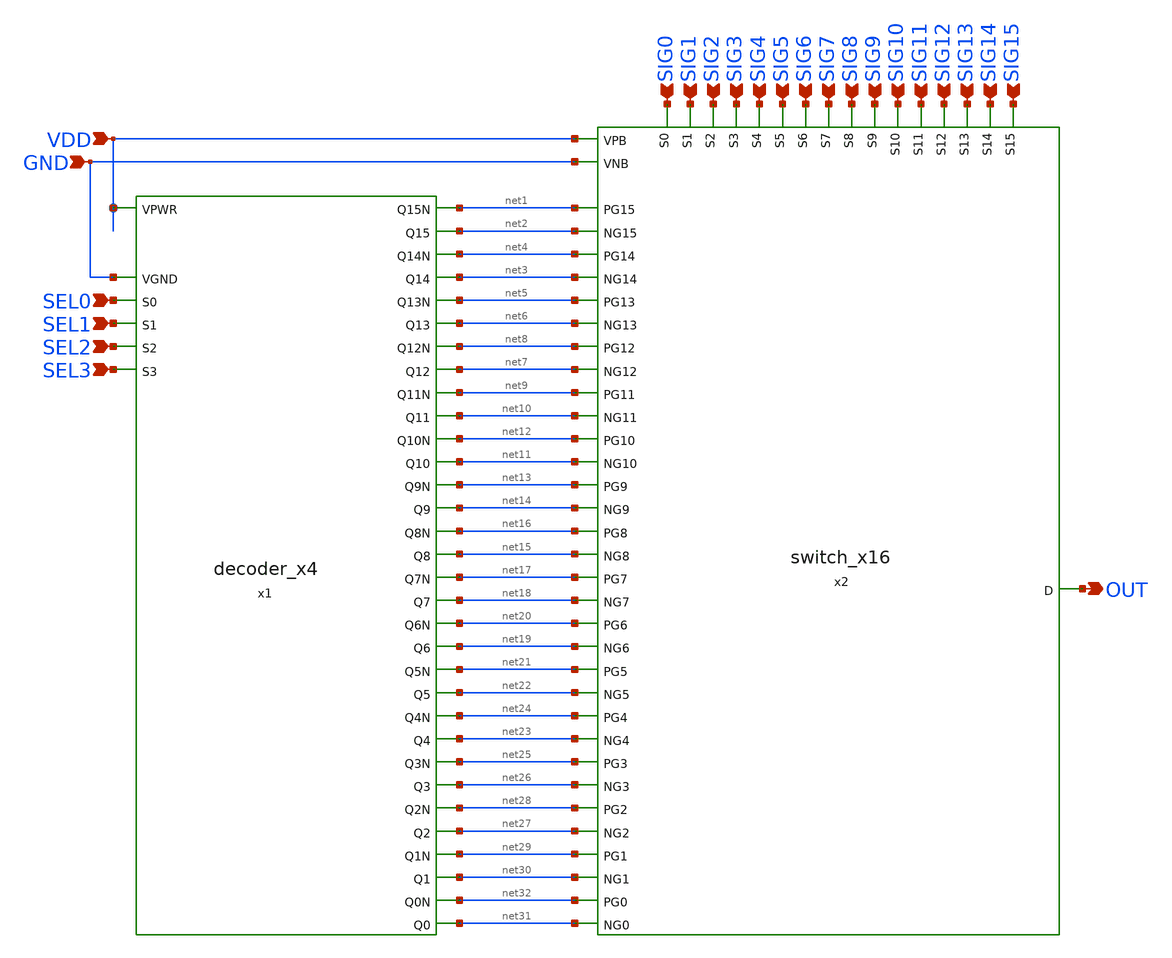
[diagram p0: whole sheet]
** sch_path: SP23_Tapeout/C2S2_Analog_TestChip-main/xschem/analog_mux.sch

.include $::SKYWATER_STDCELLS/sky130_fd_sc_hd.spice

**.subckt analog_mux OUT VDD GND SEL0 SEL1 SEL2 SEL3 SIG3 SIG2 SIG1 SIG0 SIG7 SIG6 SIG5 SIG4 SIG11
*+ SIG10 SIG9 SIG8 SIG15 SIG14 SIG13 SIG12
*.opin OUT
*.ipin VDD
*.ipin GND
*.ipin SEL0
*.ipin SEL1
*.ipin SEL2
*.ipin SEL3
*.ipin SIG3
*.ipin SIG2
*.ipin SIG1
*.ipin SIG0
*.ipin SIG7
*.ipin SIG6
*.ipin SIG5
*.ipin SIG4
*.ipin SIG11
*.ipin SIG10
*.ipin SIG9
*.ipin SIG8
*.ipin SIG15
*.ipin SIG14
*.ipin SIG13
*.ipin SIG12
x1 VDD GND SEL0 SEL1 SEL2 SEL3 net1 net2 net4 net3 net5 net6 net8 net7 net9 net10 net12 net11 net13
+ net14 net16 net15 net17 net18 net20 net19 net21 net22 net24 net23 net25 net26 net28 net27 net29 net30
+ net32 net31 decoder_x4
x2 SIG15 net1 net2 SIG14 net4 net3 SIG13 net5 net6 SIG12 net8 net7 SIG11 net9 net10 SIG10 net12
+ net11 SIG9 net13 net14 SIG8 net16 net15 OUT SIG7 net17 net18 SIG6 net20 net19 SIG5 net21 net22 SIG4 net24
+ net23 SIG3 net25 net26 SIG2 net28 net27 SIG1 net29 net30 SIG0 net32 net31 VDD GND switch_x16
**.ends

* expanding   symbol:  decoder_x4.sym # of pins=38
** sym_path: SP23_Tapeout/C2S2_Analog_TestChip-main/xschem/decoder_x4.sym
** sch_path: SP23_Tapeout/C2S2_Analog_TestChip-main/xschem/decoder_x4.sch
.subckt decoder_x4 VPWR VGND S0 S1 S2 S3 Q15N Q15 Q14N Q14 Q13N Q13 Q12N Q12 Q11N Q11 Q10N Q10 Q9N
+ Q9 Q8N Q8 Q7N Q7 Q6N Q6 Q5N Q5 Q4N Q4 Q3N Q3 Q2N Q2 Q1N Q1 Q0N Q0
*.ipin S3
*.ipin S2
*.ipin S1
*.ipin S0
*.ipin VGND
*.ipin VPWR
*.opin Q14N
*.opin Q15N
*.opin Q13N
*.opin Q12N
*.opin Q10N
*.opin Q11N
*.opin Q9N
*.opin Q8N
*.opin Q7N
*.opin Q6N
*.opin Q4N
*.opin Q3N
*.opin Q2N
*.opin Q1N
*.opin Q0N
*.opin Q5N
*.opin Q14
*.opin Q15
*.opin Q13
*.opin Q12
*.opin Q10
*.opin Q11
*.opin Q9
*.opin Q8
*.opin Q7
*.opin Q6
*.opin Q4
*.opin Q3
*.opin Q2
*.opin Q1
*.opin Q0
*.opin Q5
x17 S3 VGND VGND VPWR VPWR S3N sky130_fd_sc_hd__inv_8
x18 S2 VGND VGND VPWR VPWR S2N sky130_fd_sc_hd__inv_8
x19 S1 VGND VGND VPWR VPWR S1N sky130_fd_sc_hd__inv_8
x20 S0 VGND VGND VPWR VPWR S0N sky130_fd_sc_hd__inv_8
x21 Q0N VGND VGND VPWR VPWR Q0 sky130_fd_sc_hd__inv_2
x22 Q1N VGND VGND VPWR VPWR Q1 sky130_fd_sc_hd__inv_2
x23 Q2N VGND VGND VPWR VPWR Q2 sky130_fd_sc_hd__inv_2
x24 Q3N VGND VGND VPWR VPWR Q3 sky130_fd_sc_hd__inv_2
x1 S3N S2N S1N S0N VGND VGND VPWR VPWR Q0N sky130_fd_sc_hd__nand4_2
x2 S3N S2N S1N S0 VGND VGND VPWR VPWR Q1N sky130_fd_sc_hd__nand4_2
x3 S3N S2N S1 S0N VGND VGND VPWR VPWR Q2N sky130_fd_sc_hd__nand4_2
x4 S3N S2N S1 S0 VGND VGND VPWR VPWR Q3N sky130_fd_sc_hd__nand4_2
x5 S3N S2 S1N S0N VGND VGND VPWR VPWR Q4N sky130_fd_sc_hd__nand4_2
x6 S3N S2 S1N S0 VGND VGND VPWR VPWR Q5N sky130_fd_sc_hd__nand4_2
x7 S3N S2 S1 S0N VGND VGND VPWR VPWR Q6N sky130_fd_sc_hd__nand4_2
x8 S3N S2 S1 S0 VGND VGND VPWR VPWR Q7N sky130_fd_sc_hd__nand4_2
x9 S3 S2N S1N S0N VGND VGND VPWR VPWR Q8N sky130_fd_sc_hd__nand4_2
x10 S3 S2N S1N S0 VGND VGND VPWR VPWR Q9N sky130_fd_sc_hd__nand4_2
x11 S3 S2N S1 S0N VGND VGND VPWR VPWR Q10N sky130_fd_sc_hd__nand4_2
x12 S3 S2N S1 S0 VGND VGND VPWR VPWR Q11N sky130_fd_sc_hd__nand4_2
x13 S3 S2 S1N S0N VGND VGND VPWR VPWR Q12N sky130_fd_sc_hd__nand4_2
x14 S3 S2 S1N S0 VGND VGND VPWR VPWR Q13N sky130_fd_sc_hd__nand4_2
x15 S3 S2 S1 S0N VGND VGND VPWR VPWR Q14N sky130_fd_sc_hd__nand4_2
x16 S3 S2 S1 S0 VGND VGND VPWR VPWR Q15N sky130_fd_sc_hd__nand4_2
x25 Q4N VGND VGND VPWR VPWR Q4 sky130_fd_sc_hd__inv_2
x26 Q5N VGND VGND VPWR VPWR Q5 sky130_fd_sc_hd__inv_2
x27 Q6N VGND VGND VPWR VPWR Q6 sky130_fd_sc_hd__inv_2
x28 Q7N VGND VGND VPWR VPWR Q7 sky130_fd_sc_hd__inv_2
x29 Q8N VGND VGND VPWR VPWR Q8 sky130_fd_sc_hd__inv_2
x30 Q9N VGND VGND VPWR VPWR Q9 sky130_fd_sc_hd__inv_2
x31 Q10N VGND VGND VPWR VPWR Q10 sky130_fd_sc_hd__inv_2
x32 Q11N VGND VGND VPWR VPWR Q11 sky130_fd_sc_hd__inv_2
x33 Q12N VGND VGND VPWR VPWR Q12 sky130_fd_sc_hd__inv_2
x34 Q13N VGND VGND VPWR VPWR Q13 sky130_fd_sc_hd__inv_2
x35 Q14N VGND VGND VPWR VPWR Q14 sky130_fd_sc_hd__inv_2
x36 Q15N VGND VGND VPWR VPWR Q15 sky130_fd_sc_hd__inv_2
.ends


* expanding   symbol:  switch_x16.sym # of pins=51
** sym_path: switch_x16.sym
** sch_path: switch_x16.sch
.subckt switch_x16 S15 PG15 NG15 S14 PG14 NG14 S13 PG13 NG13 S12 PG12 NG12 S11 PG11 NG11 S10 PG10
+ NG10 S9 PG9 NG9 S8 PG8 NG8 D S7 PG7 NG7 S6 PG6 NG6 S5 PG5 NG5 S4 PG4 NG4 S3 PG3 NG3 S2 PG2 NG2 S1 PG1
+ NG1 S0 PG0 NG0 VPB VNB
*.ipin PG0
*.ipin NG0
*.ipin S0
*.ipin PG1
*.ipin NG1
*.ipin S1
*.ipin PG2
*.ipin NG2
*.ipin S2
*.ipin PG3
*.ipin NG3
*.ipin S3
*.ipin PG4
*.ipin NG4
*.ipin S4
*.ipin PG5
*.ipin NG5
*.ipin S5
*.ipin PG6
*.ipin NG6
*.ipin S6
*.ipin PG7
*.ipin NG7
*.ipin S7
*.ipin PG8
*.ipin NG8
*.ipin S8
*.ipin PG9
*.ipin NG9
*.ipin S9
*.ipin PG10
*.ipin NG10
*.ipin S10
*.ipin PG11
*.ipin NG11
*.ipin S11
*.ipin PG12
*.ipin NG12
*.ipin S12
*.ipin PG13
*.ipin NG13
*.ipin S13
*.ipin PG14
*.ipin NG14
*.ipin S14
*.ipin PG15
*.ipin NG15
*.ipin S15
*.opin D
*.ipin VPB
*.ipin VNB
x1 S0 VNB NG0 VPB PG0 D a_mux_switch
x2 S1 VNB NG1 VPB PG1 D a_mux_switch
x3 S2 VNB NG2 VPB PG2 D a_mux_switch
x4 S3 VNB NG3 VPB PG3 D a_mux_switch
x5 S4 VNB NG4 VPB PG4 D a_mux_switch
x6 S5 VNB NG5 VPB PG5 D a_mux_switch
x7 S6 VNB NG6 VPB PG6 D a_mux_switch
x8 S7 VNB NG7 VPB PG7 D a_mux_switch
x9 S8 VNB NG8 VPB PG8 D a_mux_switch
x10 S9 VNB NG9 VPB PG9 D a_mux_switch
x11 S10 VNB NG10 VPB PG10 D a_mux_switch
x15 S11 VNB NG11 VPB PG11 D a_mux_switch
x16 S12 VNB NG12 VPB PG12 D a_mux_switch
x17 S13 VNB NG13 VPB PG13 D a_mux_switch
x18 S14 VNB NG14 VPB PG14 D a_mux_switch
x19 S15 VNB NG15 VPB PG15 D a_mux_switch
.ends


* expanding   symbol:  a_mux_switch.sym # of pins=6
** sym_path: SP23_Tapeout/C2S2_Analog_TestChip-main/xschem/a_mux_switch.sym
** sch_path: SP23_Tapeout/C2S2_Analog_TestChip-main/xschem/a_mux_switch.sch
.subckt a_mux_switch VD VNB VNG VPB VPG VS
*.ipin VPG
*.ipin VNG
*.ipin VD
*.opin VS
*.ipin VPB
*.ipin VNB
XM1 VD VPG VS VPB sky130_fd_pr__pfet_01v8 L=0.15 W=95 nf=19 ad='int((nf+1)/2) * W/nf * 0.29' as='int((nf+2)/2) * W/nf * 0.29'
+ pd='2*int((nf+1)/2) * (W/nf + 0.29)' ps='2*int((nf+2)/2) * (W/nf + 0.29)' nrd='0.29 / W' nrs='0.29 / W'
+ sa=0 sb=0 sd=0 mult=1 m=1
XM2 VD VNG VS VNB sky130_fd_pr__nfet_01v8 L=0.15 W=45 nf=9 ad='int((nf+1)/2) * W/nf * 0.29' as='int((nf+2)/2) * W/nf * 0.29'
+ pd='2*int((nf+1)/2) * (W/nf + 0.29)' ps='2*int((nf+2)/2) * (W/nf + 0.29)' nrd='0.29 / W' nrs='0.29 / W'
+ sa=0 sb=0 sd=0 mult=1 m=1
.ends

.GLOBAL VPB
.GLOBAL VNB
.end
